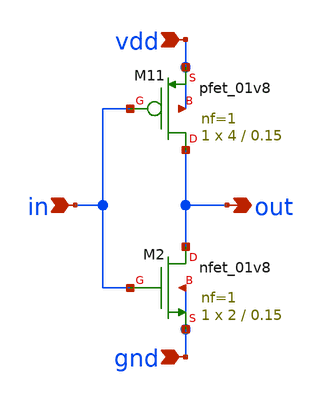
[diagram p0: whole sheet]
** sch_path: pll/dividers_lib/divider_init/xschem/inv.sch
**.subckt inv vdd in gnd out
*.ipin vdd
*.ipin in
*.ipin gnd
*.opin out
XM11 out in vdd vdd sky130_fd_pr__pfet_01v8 L=0.15 W=4 nf=1 ad='int((nf+1)/2) * W/nf * 0.29' as='int((nf+2)/2) * W/nf * 0.29'
+ pd='2*int((nf+1)/2) * (W/nf + 0.29)' ps='2*int((nf+2)/2) * (W/nf + 0.29)' nrd='0.29 / W' nrs='0.29 / W'
+ sa=0 sb=0 sd=0 mult=1 m=1
XM2 out in gnd gnd sky130_fd_pr__nfet_01v8 L=0.15 W=2 nf=1 ad='int((1 + 1)/2) * 2 / 1 * 0.29' as='int((1 + 2)/2) * 2 / 1 * 0.29'
+ pd='2*int((1 + 1)/2) * (2 / 1 + 0.29)' ps='2*int((1 + 2)/2) * (2 / 1 + 0.29)' nrd='0.29 / 2 ' nrs='0.29 / 2 '
+ sa=0 sb=0 sd=0 mult=1 m=1
**.ends
.end
